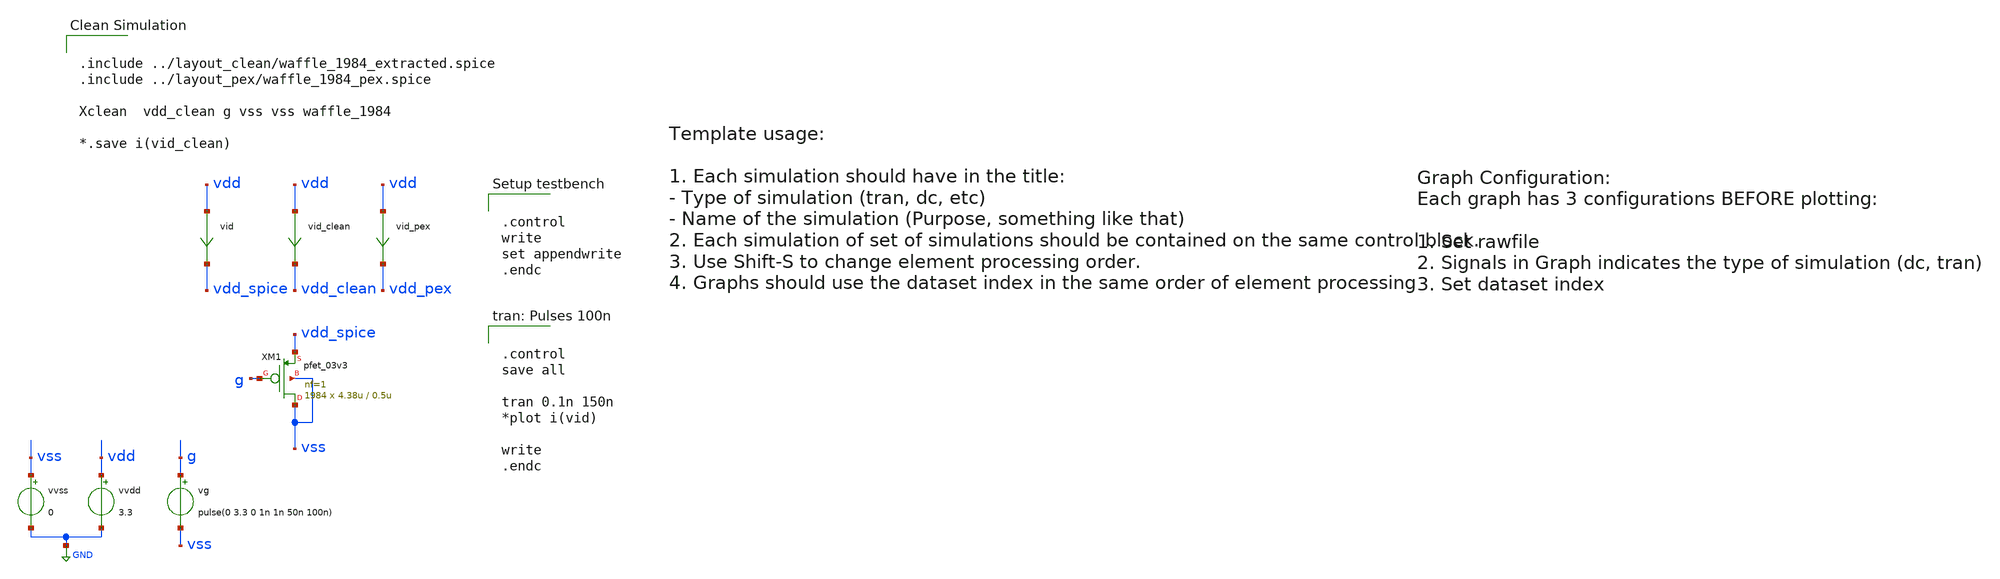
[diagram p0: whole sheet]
** sch_path: LDO/xschem/waffle_1984/test/waffle_1984_test.sch

.include $env(PDK_ROOT)/$env(PDK)/libs.tech/ngspice/design.ngspice
.lib $env(PDK_ROOT)/$env(PDK)/libs.tech/ngspice/sm141064.ngspice typical
.lib $env(PDK_ROOT)/$env(PDK)/libs.tech/ngspice/sm141064.ngspice mimcap_statistical
.lib $env(PDK_ROOT)/$env(PDK)/libs.tech/ngspice/sm141064.ngspice cap_mim
.lib $env(PDK_ROOT)/$env(PDK)/libs.tech/ngspice/sm141064.ngspice res_typical
.lib $env(PDK_ROOT)/$env(PDK)/libs.tech/ngspice/sm141064.ngspice bjt_typical
.lib $env(PDK_ROOT)/$env(PDK)/libs.tech/ngspice/sm141064.ngspice moscap_typical


.control
write
set appendwrite
.endc


**.subckt waffle_1984_test
vvdd vdd GND 3.3
vg g vss pulse(0 3.3 0 1n 1n 50n 100n)
vvss vss GND 0
vid vdd vdd_spice 0
.save i(vid)
XM1 vss g vdd_spice vss pfet_03v3 L=0.5u W=4.38u nf=1 ad='int((nf+1)/2) * W/nf * 0.18u' as='int((nf+2)/2) * W/nf * 0.18u'
+ pd='2*int((nf+1)/2) * (W/nf + 0.18u)' ps='2*int((nf+2)/2) * (W/nf + 0.18u)' nrd='0.18u / W' nrs='0.18u / W'
+ sa=0 sb=0 sd=0 m=1984
vid_clean vdd vdd_clean 0
.save i(vid_clean)
vid_pex vdd vdd_pex 0
.save i(vid_pex)
**** begin user architecture code


.control
save all

tran 0.1n 150n
*plot i(vid)

write
.endc




.include ../layout_clean/waffle_1984_extracted.spice
.include ../layout_pex/waffle_1984_pex.spice

Xclean  vdd_clean g vss vss waffle_1984

*.save i(vid_clean)




.control
save all

dc vvdd 0 3.3 0.01 vg 0 3.3 0.5

plot i(vid) i(vid_clean)

write

.endc


**** end user architecture code
**.ends
.GLOBAL GND
.end
